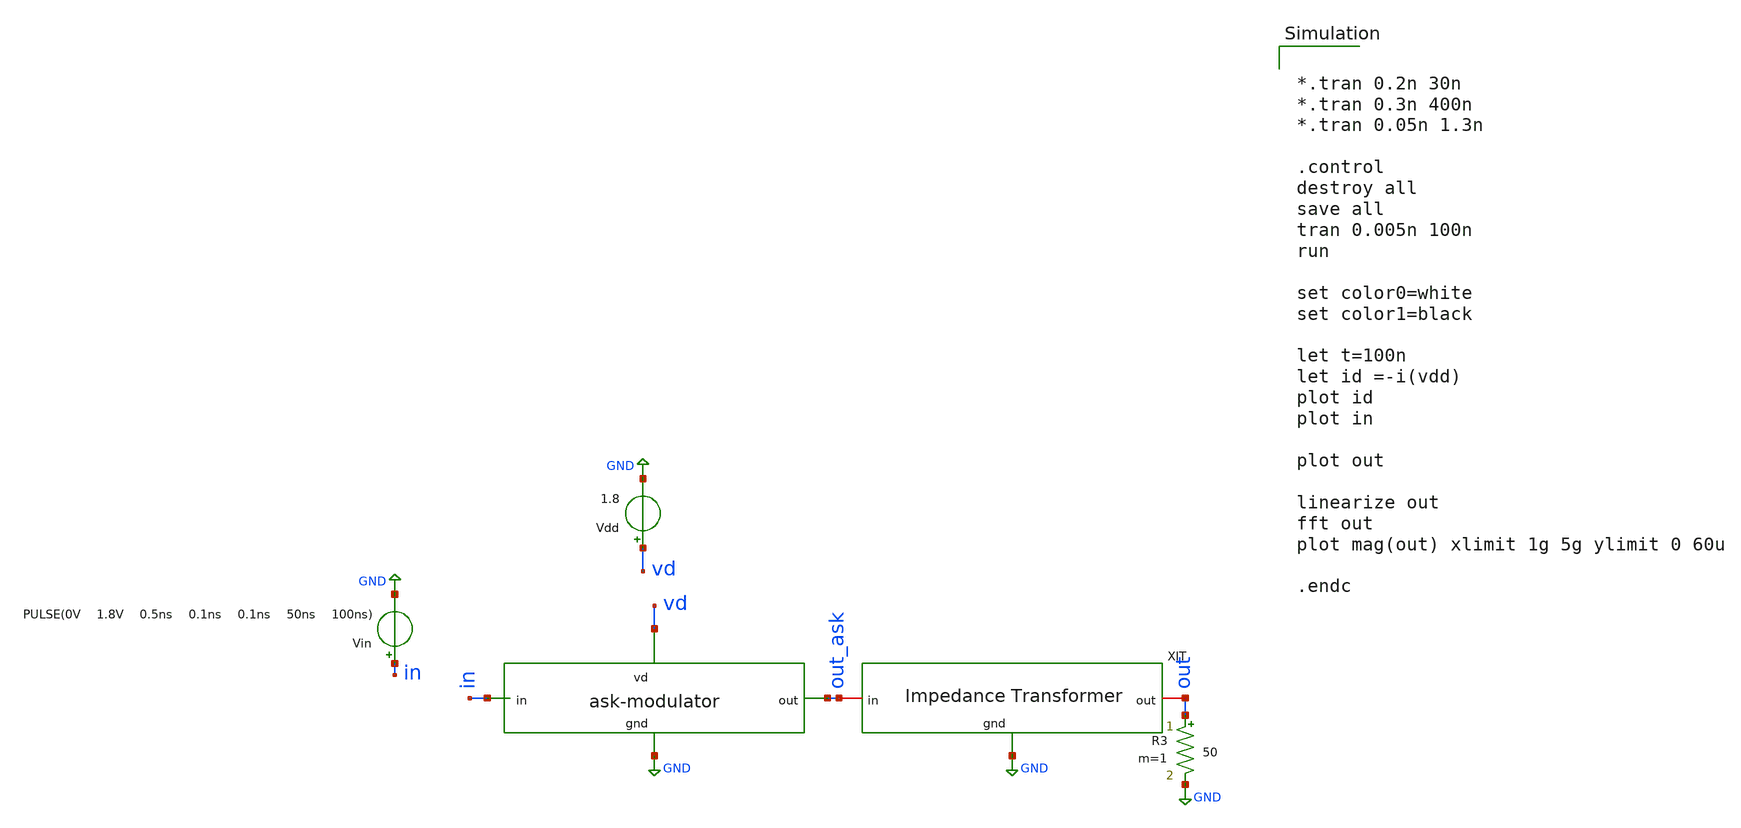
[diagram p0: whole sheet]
** sch_path: impedance-transformer/xschem/impedance-transformer_tb-tran.sch
**.subckt impedance-transformer_tb-tran
Vdd vd GND 1.8
Vin in GND PULSE(0V 1.8V 0.5ns 0.1ns 0.1ns 50ns 100ns)
x1 vd out_ask in GND ask-modulator
x2 out_ask out GND impedance-transformer
R3 out GND 50 m=1
**** begin user architecture code


*.tran 0.2n 30n
*.tran 0.3n 400n
*.tran 0.05n 1.3n

.control
destroy all
save all
tran 0.005n 100n
run

set color0=white
set color1=black

let t=100n
let id =-i(vdd)
plot id
plot in

plot out

linearize out
fft out
plot mag(out) xlimit 1g 5g ylimit 0 60u

.endc

 .lib $::SKYWATER_MODELS/sky130.lib.spice tt
.include $::SKYWATER_STDCELLS/sky130_fd_sc_hd.spice

**** end user architecture code
**.ends
.GLOBAL GND
.end
